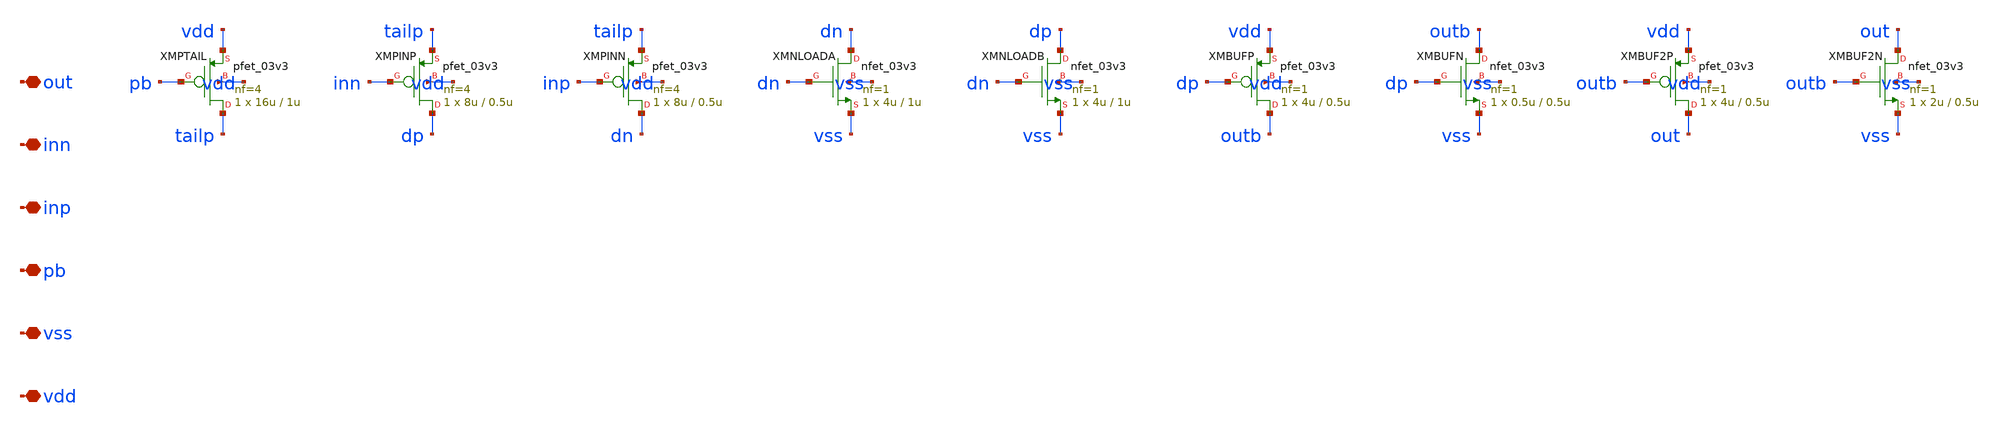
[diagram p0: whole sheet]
** sch_path: design/rcosc_comparator_p.sch
**.subckt rcosc_comparator_p vdd vss pb inp inn out
*.iopin vdd
*.iopin vss
*.iopin pb
*.iopin inp
*.iopin inn
*.iopin out
XMPTAIL tailp pb vdd vdd pfet_03v3 L=1u W=16u nf=4 ad='int((nf+1)/2) * W/nf * 0.18u' as='int((nf+2)/2) * W/nf * 0.18u'
+ pd='2*int((nf+1)/2) * (W/nf + 0.18u)' ps='2*int((nf+2)/2) * (W/nf + 0.18u)' nrd='0.18u / W' nrs='0.18u / W'
+ sa=0 sb=0 sd=0 m=1
XMPINP dp inn tailp vdd pfet_03v3 L=0.5u W=8u nf=4 ad='int((nf+1)/2) * W/nf * 0.18u' as='int((nf+2)/2) * W/nf * 0.18u'
+ pd='2*int((nf+1)/2) * (W/nf + 0.18u)' ps='2*int((nf+2)/2) * (W/nf + 0.18u)' nrd='0.18u / W' nrs='0.18u / W'
+ sa=0 sb=0 sd=0 m=1
XMPINN dn inp tailp vdd pfet_03v3 L=0.5u W=8u nf=4 ad='int((nf+1)/2) * W/nf * 0.18u' as='int((nf+2)/2) * W/nf * 0.18u'
+ pd='2*int((nf+1)/2) * (W/nf + 0.18u)' ps='2*int((nf+2)/2) * (W/nf + 0.18u)' nrd='0.18u / W' nrs='0.18u / W'
+ sa=0 sb=0 sd=0 m=1
XMNLOADA dn dn vss vss nfet_03v3 L=1u W=4u nf=1 ad='int((nf+1)/2) * W/nf * 0.18u' as='int((nf+2)/2) * W/nf * 0.18u'
+ pd='2*int((nf+1)/2) * (W/nf + 0.18u)' ps='2*int((nf+2)/2) * (W/nf + 0.18u)' nrd='0.18u / W' nrs='0.18u / W'
+ sa=0 sb=0 sd=0 m=1
XMNLOADB dp dn vss vss nfet_03v3 L=1u W=4u nf=1 ad='int((nf+1)/2) * W/nf * 0.18u' as='int((nf+2)/2) * W/nf * 0.18u'
+ pd='2*int((nf+1)/2) * (W/nf + 0.18u)' ps='2*int((nf+2)/2) * (W/nf + 0.18u)' nrd='0.18u / W' nrs='0.18u / W'
+ sa=0 sb=0 sd=0 m=1
XMBUFP outb dp vdd vdd pfet_03v3 L=0.5u W=4u nf=1 ad='int((nf+1)/2) * W/nf * 0.18u' as='int((nf+2)/2) * W/nf * 0.18u'
+ pd='2*int((nf+1)/2) * (W/nf + 0.18u)' ps='2*int((nf+2)/2) * (W/nf + 0.18u)' nrd='0.18u / W' nrs='0.18u / W'
+ sa=0 sb=0 sd=0 m=1
XMBUFN outb dp vss vss nfet_03v3 L=0.5u W=0.5u nf=1 ad='int((nf+1)/2) * W/nf * 0.18u' as='int((nf+2)/2) * W/nf * 0.18u'
+ pd='2*int((nf+1)/2) * (W/nf + 0.18u)' ps='2*int((nf+2)/2) * (W/nf + 0.18u)' nrd='0.18u / W' nrs='0.18u / W'
+ sa=0 sb=0 sd=0 m=1
XMBUF2P out outb vdd vdd pfet_03v3 L=0.5u W=4u nf=1 ad='int((nf+1)/2) * W/nf * 0.18u' as='int((nf+2)/2) * W/nf * 0.18u'
+ pd='2*int((nf+1)/2) * (W/nf + 0.18u)' ps='2*int((nf+2)/2) * (W/nf + 0.18u)' nrd='0.18u / W' nrs='0.18u / W'
+ sa=0 sb=0 sd=0 m=1
XMBUF2N out outb vss vss nfet_03v3 L=0.5u W=2u nf=1 ad='int((nf+1)/2) * W/nf * 0.18u' as='int((nf+2)/2) * W/nf * 0.18u'
+ pd='2*int((nf+1)/2) * (W/nf + 0.18u)' ps='2*int((nf+2)/2) * (W/nf + 0.18u)' nrd='0.18u / W' nrs='0.18u / W'
+ sa=0 sb=0 sd=0 m=1
**.ends
.end
